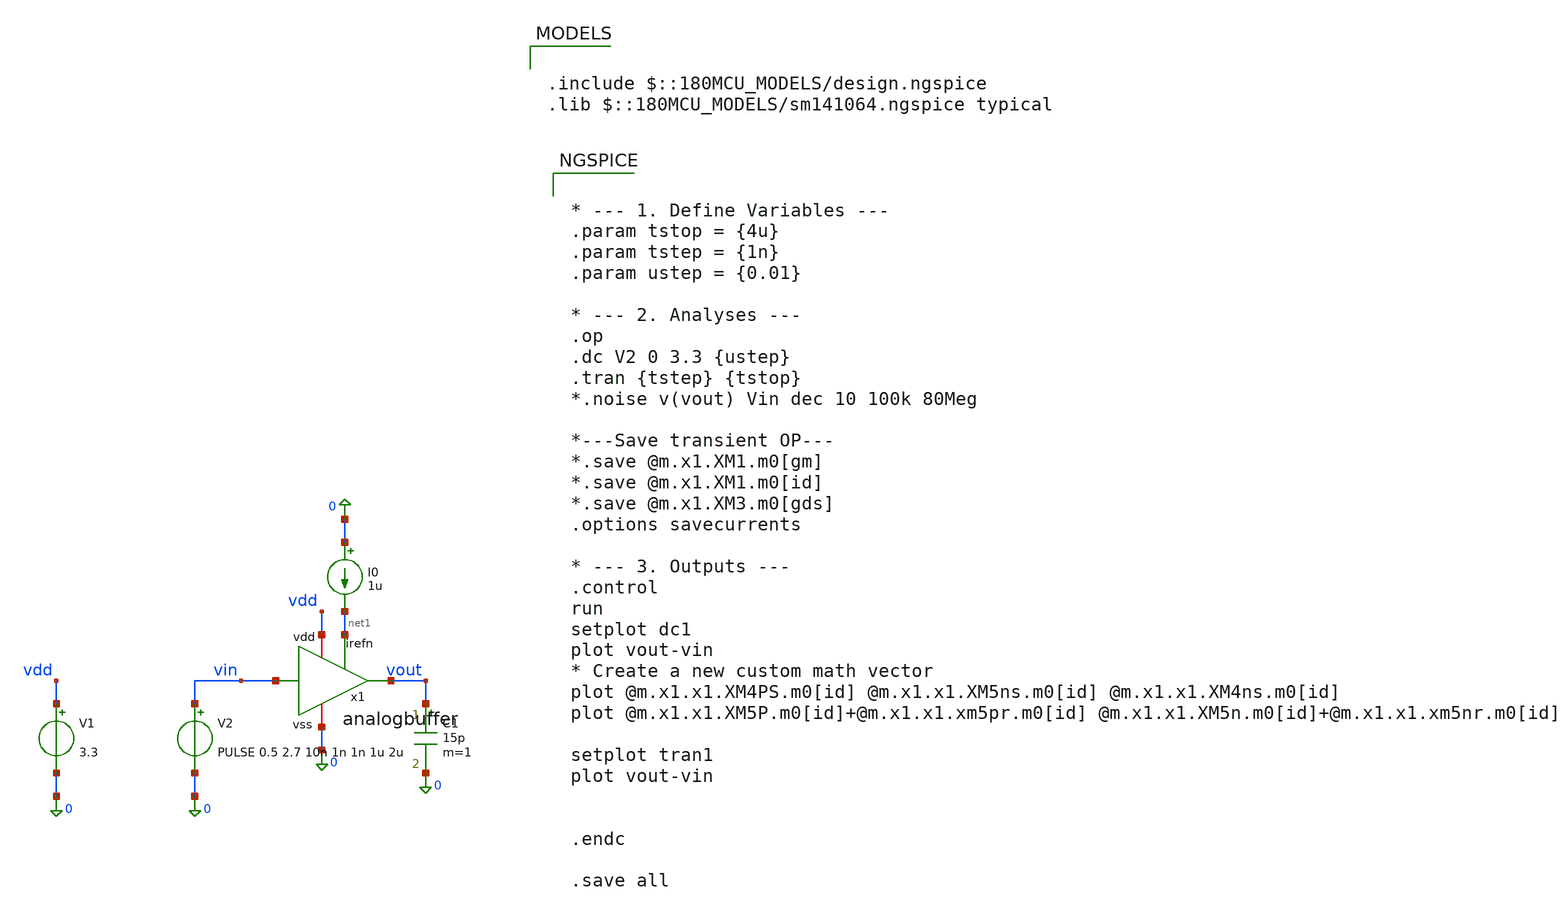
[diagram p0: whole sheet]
** sch_path: Tobias/2026 07 17 Results/analogbuffer/analogbuffer-tb.sch
**.subckt analogbuffer-tb
x1 vdd net1 vin vout 0 analogbuffer
I0 0 net1 1u
V1 vdd 0 3.3
V2 vin 0 PULSE 0.5 2.7 10n 1n 1n 1u 2u
C1 vout 0 15p m=1
**** begin user architecture code


* --- 1. Define Variables ---
.param tstop = {4u}
.param tstep = {1n}
.param ustep = {0.01}

* --- 2. Analyses ---
.op
.dc V2 0 3.3 {ustep}
.tran {tstep} {tstop}
*.noise v(vout) Vin dec 10 100k 80Meg

*---Save transient OP---
*.save @m.x1.XM1.m0[gm]
*.save @m.x1.XM1.m0[id]
*.save @m.x1.XM3.m0[gds]
.options savecurrents

* --- 3. Outputs ---
.control
run
setplot dc1
plot vout-vin
* Create a new custom math vector
plot @m.x1.x1.XM4PS.m0[id] @m.x1.x1.XM5ns.m0[id] @m.x1.x1.XM4ns.m0[id]
plot @m.x1.x1.XM5P.m0[id]+@m.x1.x1.xm5pr.m0[id] @m.x1.x1.XM5n.m0[id]+@m.x1.x1.xm5nr.m0[id]

setplot tran1
plot vout-vin


.endc

.save all



.include $::180MCU_MODELS/design.ngspice
.lib $::180MCU_MODELS/sm141064.ngspice typical

**** end user architecture code
**.ends

* expanding   symbol:  analogbuffer/analogbuffer.sym # of pins=5
** sym_path: Tobias/2026 07 17 Results/analogbuffer/analogbuffer.sym
** sch_path: Tobias/2026 07 17 Results/analogbuffer/analogbuffer.sch
.subckt analogbuffer vdd irefn vin vout vss
*.iopin vdd
*.iopin vss
*.ipin irefn
*.ipin vin
*.opin vout
x1 vdd irefn vin vout vout vss analogbuffer-openloop
.ends


* expanding   symbol:  analogbuffer/analogbuffer-openloop.sym # of pins=6
** sym_path: Tobias/2026 07 17 Results/analogbuffer/analogbuffer-openloop.sym
** sch_path: Tobias/2026 07 17 Results/analogbuffer/analogbuffer-openloop.sch
.subckt analogbuffer-openloop vdd irefn vin_p vout vin_n vss
*.iopin vdd
*.iopin vss
*.ipin vin_p
*.opin vout
*.ipin irefn
*.ipin vin_n
XM2P net7 vin_p net10 vdd pfet_03v3 L=4u W=80u nf=1 ad='int((nf+1)/2) * W/nf * 0.18u' as='int((nf+2)/2) * W/nf * 0.18u'
+ pd='2*int((nf+1)/2) * (W/nf + 0.18u)' ps='2*int((nf+2)/2) * (W/nf + 0.18u)' nrd='0.18u / W' nrs='0.18u / W'
+ sa=0 sb=0 sd=0 m=1
XM2N net1 vin_p net4 vss nfet_03v3 L=4u W=40u nf=1 ad='int((nf+1)/2) * W/nf * 0.18u' as='int((nf+2)/2) * W/nf * 0.18u'
+ pd='2*int((nf+1)/2) * (W/nf + 0.18u)' ps='2*int((nf+2)/2) * (W/nf + 0.18u)' nrd='0.18u / W' nrs='0.18u / W'
+ sa=0 sb=0 sd=0 m=1
XM3N net4 net8 vss vss nfet_03v3 L=4u W=2u nf=1 ad='int((nf+1)/2) * W/nf * 0.18u' as='int((nf+2)/2) * W/nf * 0.18u'
+ pd='2*int((nf+1)/2) * (W/nf + 0.18u)' ps='2*int((nf+2)/2) * (W/nf + 0.18u)' nrd='0.18u / W' nrs='0.18u / W'
+ sa=0 sb=0 sd=0 m=1
XM1NR net3 vin_n net4 vss nfet_03v3 L=4u W=40u nf=1 ad='int((nf+1)/2) * W/nf * 0.18u' as='int((nf+2)/2) * W/nf * 0.18u'
+ pd='2*int((nf+1)/2) * (W/nf + 0.18u)' ps='2*int((nf+2)/2) * (W/nf + 0.18u)' nrd='0.18u / W' nrs='0.18u / W'
+ sa=0 sb=0 sd=0 m=1
XM2NR net3 net3 vdd vdd pfet_03v3 L=2u W=4u nf=1 ad='int((nf+1)/2) * W/nf * 0.18u' as='int((nf+2)/2) * W/nf * 0.18u'
+ pd='2*int((nf+1)/2) * (W/nf + 0.18u)' ps='2*int((nf+2)/2) * (W/nf + 0.18u)' nrd='0.18u / W' nrs='0.18u / W'
+ sa=0 sb=0 sd=0 m=1
XM3NR net2 net3 vdd vdd pfet_03v3 L=2u W=4u nf=1 ad='int((nf+1)/2) * W/nf * 0.18u' as='int((nf+2)/2) * W/nf * 0.18u'
+ pd='2*int((nf+1)/2) * (W/nf + 0.18u)' ps='2*int((nf+2)/2) * (W/nf + 0.18u)' nrd='0.18u / W' nrs='0.18u / W'
+ sa=0 sb=0 sd=0 m=1
XM4NR net2 net2 vdd vdd pfet_03v3 L=2u W=4u nf=1 ad='int((nf+1)/2) * W/nf * 0.18u' as='int((nf+2)/2) * W/nf * 0.18u'
+ pd='2*int((nf+1)/2) * (W/nf + 0.18u)' ps='2*int((nf+2)/2) * (W/nf + 0.18u)' nrd='0.18u / W' nrs='0.18u / W'
+ sa=0 sb=0 sd=0 m=1
XM5NR vout net2 vdd vdd pfet_03v3 L=2u W=40u nf=1 ad='int((nf+1)/2) * W/nf * 0.18u' as='int((nf+2)/2) * W/nf * 0.18u'
+ pd='2*int((nf+1)/2) * (W/nf + 0.18u)' ps='2*int((nf+2)/2) * (W/nf + 0.18u)' nrd='0.18u / W' nrs='0.18u / W'
+ sa=0 sb=0 sd=0 m=1
XM5N vout net1 vdd vdd pfet_03v3 L=2u W=40u nf=1 ad='int((nf+1)/2) * W/nf * 0.18u' as='int((nf+2)/2) * W/nf * 0.18u'
+ pd='2*int((nf+1)/2) * (W/nf + 0.18u)' ps='2*int((nf+2)/2) * (W/nf + 0.18u)' nrd='0.18u / W' nrs='0.18u / W'
+ sa=0 sb=0 sd=0 m=1
XM4N net1 net1 vdd vdd pfet_03v3 L=2u W=4u nf=1 ad='int((nf+1)/2) * W/nf * 0.18u' as='int((nf+2)/2) * W/nf * 0.18u'
+ pd='2*int((nf+1)/2) * (W/nf + 0.18u)' ps='2*int((nf+2)/2) * (W/nf + 0.18u)' nrd='0.18u / W' nrs='0.18u / W'
+ sa=0 sb=0 sd=0 m=1
XM5NS net2 irefn vss vss nfet_03v3 L=2u W=2u nf=1 ad='int((nf+1)/2) * W/nf * 0.18u' as='int((nf+2)/2) * W/nf * 0.18u'
+ pd='2*int((nf+1)/2) * (W/nf + 0.18u)' ps='2*int((nf+2)/2) * (W/nf + 0.18u)' nrd='0.18u / W' nrs='0.18u / W'
+ sa=0 sb=0 sd=0 m=1
XM1PR net5 vin_n net10 vdd pfet_03v3 L=4u W=80u nf=1 ad='int((nf+1)/2) * W/nf * 0.18u' as='int((nf+2)/2) * W/nf * 0.18u'
+ pd='2*int((nf+1)/2) * (W/nf + 0.18u)' ps='2*int((nf+2)/2) * (W/nf + 0.18u)' nrd='0.18u / W' nrs='0.18u / W'
+ sa=0 sb=0 sd=0 m=1
XM3P net10 net9 vdd vdd pfet_03v3 L=4u W=4u nf=1 ad='int((nf+1)/2) * W/nf * 0.18u' as='int((nf+2)/2) * W/nf * 0.18u'
+ pd='2*int((nf+1)/2) * (W/nf + 0.18u)' ps='2*int((nf+2)/2) * (W/nf + 0.18u)' nrd='0.18u / W' nrs='0.18u / W'
+ sa=0 sb=0 sd=0 m=1
XM2PR net5 net5 vss vss nfet_03v3 L=2u W=2u nf=1 ad='int((nf+1)/2) * W/nf * 0.18u' as='int((nf+2)/2) * W/nf * 0.18u'
+ pd='2*int((nf+1)/2) * (W/nf + 0.18u)' ps='2*int((nf+2)/2) * (W/nf + 0.18u)' nrd='0.18u / W' nrs='0.18u / W'
+ sa=0 sb=0 sd=0 m=1
XM3PR net6 net5 vss vss nfet_03v3 L=2u W=2u nf=1 ad='int((nf+1)/2) * W/nf * 0.18u' as='int((nf+2)/2) * W/nf * 0.18u'
+ pd='2*int((nf+1)/2) * (W/nf + 0.18u)' ps='2*int((nf+2)/2) * (W/nf + 0.18u)' nrd='0.18u / W' nrs='0.18u / W'
+ sa=0 sb=0 sd=0 m=1
XM4PR net6 net6 vss vss nfet_03v3 L=2u W=2u nf=1 ad='int((nf+1)/2) * W/nf * 0.18u' as='int((nf+2)/2) * W/nf * 0.18u'
+ pd='2*int((nf+1)/2) * (W/nf + 0.18u)' ps='2*int((nf+2)/2) * (W/nf + 0.18u)' nrd='0.18u / W' nrs='0.18u / W'
+ sa=0 sb=0 sd=0 m=1
XM5PR vout net6 vss vss nfet_03v3 L=2u W=20u nf=1 ad='int((nf+1)/2) * W/nf * 0.18u' as='int((nf+2)/2) * W/nf * 0.18u'
+ pd='2*int((nf+1)/2) * (W/nf + 0.18u)' ps='2*int((nf+2)/2) * (W/nf + 0.18u)' nrd='0.18u / W' nrs='0.18u / W'
+ sa=0 sb=0 sd=0 m=1
XM5PS net6 irefp vdd vdd pfet_03v3 L=2u W=4u nf=1 ad='int((nf+1)/2) * W/nf * 0.18u' as='int((nf+2)/2) * W/nf * 0.18u'
+ pd='2*int((nf+1)/2) * (W/nf + 0.18u)' ps='2*int((nf+2)/2) * (W/nf + 0.18u)' nrd='0.18u / W' nrs='0.18u / W'
+ sa=0 sb=0 sd=0 m=1
XM5P vout net7 vss vss nfet_03v3 L=2u W=20u nf=1 ad='int((nf+1)/2) * W/nf * 0.18u' as='int((nf+2)/2) * W/nf * 0.18u'
+ pd='2*int((nf+1)/2) * (W/nf + 0.18u)' ps='2*int((nf+2)/2) * (W/nf + 0.18u)' nrd='0.18u / W' nrs='0.18u / W'
+ sa=0 sb=0 sd=0 m=1
XM4P net7 net7 vss vss nfet_03v3 L=2u W=2u nf=1 ad='int((nf+1)/2) * W/nf * 0.18u' as='int((nf+2)/2) * W/nf * 0.18u'
+ pd='2*int((nf+1)/2) * (W/nf + 0.18u)' ps='2*int((nf+2)/2) * (W/nf + 0.18u)' nrd='0.18u / W' nrs='0.18u / W'
+ sa=0 sb=0 sd=0 m=1
XM2NS irefp irefn vss vss nfet_03v3 L=2u W=1u nf=1 ad='int((nf+1)/2) * W/nf * 0.18u' as='int((nf+2)/2) * W/nf * 0.18u'
+ pd='2*int((nf+1)/2) * (W/nf + 0.18u)' ps='2*int((nf+2)/2) * (W/nf + 0.18u)' nrd='0.18u / W' nrs='0.18u / W'
+ sa=0 sb=0 sd=0 m=1
XM1NS irefn irefn vss vss nfet_03v3 L=2u W=1u nf=1 ad='int((nf+1)/2) * W/nf * 0.18u' as='int((nf+2)/2) * W/nf * 0.18u'
+ pd='2*int((nf+1)/2) * (W/nf + 0.18u)' ps='2*int((nf+2)/2) * (W/nf + 0.18u)' nrd='0.18u / W' nrs='0.18u / W'
+ sa=0 sb=0 sd=0 m=1
XM2PS irefp irefp vdd vdd pfet_03v3 L=2u W=2u nf=1 ad='int((nf+1)/2) * W/nf * 0.18u' as='int((nf+2)/2) * W/nf * 0.18u'
+ pd='2*int((nf+1)/2) * (W/nf + 0.18u)' ps='2*int((nf+2)/2) * (W/nf + 0.18u)' nrd='0.18u / W' nrs='0.18u / W'
+ sa=0 sb=0 sd=0 m=1
XMSN vdd net11 net8 vss nfet_03v3 L=2u W=2u nf=1 ad='int((nf+1)/2) * W/nf * 0.18u' as='int((nf+2)/2) * W/nf * 0.18u'
+ pd='2*int((nf+1)/2) * (W/nf + 0.18u)' ps='2*int((nf+2)/2) * (W/nf + 0.18u)' nrd='0.18u / W' nrs='0.18u / W'
+ sa=0 sb=0 sd=0 m=1
XM3NS net8 irefn vss vss nfet_03v3 L=2u W=2u nf=1 ad='int((nf+1)/2) * W/nf * 0.18u' as='int((nf+2)/2) * W/nf * 0.18u'
+ pd='2*int((nf+1)/2) * (W/nf + 0.18u)' ps='2*int((nf+2)/2) * (W/nf + 0.18u)' nrd='0.18u / W' nrs='0.18u / W'
+ sa=0 sb=0 sd=0 m=1
XM1N net11 vin_n net4 vss nfet_03v3 L=4u W=40u nf=1 ad='int((nf+1)/2) * W/nf * 0.18u' as='int((nf+2)/2) * W/nf * 0.18u'
+ pd='2*int((nf+1)/2) * (W/nf + 0.18u)' ps='2*int((nf+2)/2) * (W/nf + 0.18u)' nrd='0.18u / W' nrs='0.18u / W'
+ sa=0 sb=0 sd=0 m=1
XM4PS net11 irefp vdd vdd pfet_03v3 L=2u W=4u nf=1 ad='int((nf+1)/2) * W/nf * 0.18u' as='int((nf+2)/2) * W/nf * 0.18u'
+ pd='2*int((nf+1)/2) * (W/nf + 0.18u)' ps='2*int((nf+2)/2) * (W/nf + 0.18u)' nrd='0.18u / W' nrs='0.18u / W'
+ sa=0 sb=0 sd=0 m=1
XM3PS net9 irefp vdd vdd pfet_03v3 L=2u W=4u nf=1 ad='int((nf+1)/2) * W/nf * 0.18u' as='int((nf+2)/2) * W/nf * 0.18u'
+ pd='2*int((nf+1)/2) * (W/nf + 0.18u)' ps='2*int((nf+2)/2) * (W/nf + 0.18u)' nrd='0.18u / W' nrs='0.18u / W'
+ sa=0 sb=0 sd=0 m=1
XM1P net12 vin_n net10 vdd pfet_03v3 L=4u W=80u nf=1 ad='int((nf+1)/2) * W/nf * 0.18u' as='int((nf+2)/2) * W/nf * 0.18u'
+ pd='2*int((nf+1)/2) * (W/nf + 0.18u)' ps='2*int((nf+2)/2) * (W/nf + 0.18u)' nrd='0.18u / W' nrs='0.18u / W'
+ sa=0 sb=0 sd=0 m=1
XM4NS net12 irefn vss vss nfet_03v3 L=2u W=2u nf=1 ad='int((nf+1)/2) * W/nf * 0.18u' as='int((nf+2)/2) * W/nf * 0.18u'
+ pd='2*int((nf+1)/2) * (W/nf + 0.18u)' ps='2*int((nf+2)/2) * (W/nf + 0.18u)' nrd='0.18u / W' nrs='0.18u / W'
+ sa=0 sb=0 sd=0 m=1
XMSP vss net12 net9 vdd pfet_03v3 L=1u W=4u nf=1 ad='int((nf+1)/2) * W/nf * 0.18u' as='int((nf+2)/2) * W/nf * 0.18u'
+ pd='2*int((nf+1)/2) * (W/nf + 0.18u)' ps='2*int((nf+2)/2) * (W/nf + 0.18u)' nrd='0.18u / W' nrs='0.18u / W'
+ sa=0 sb=0 sd=0 m=1
.ends

.end
